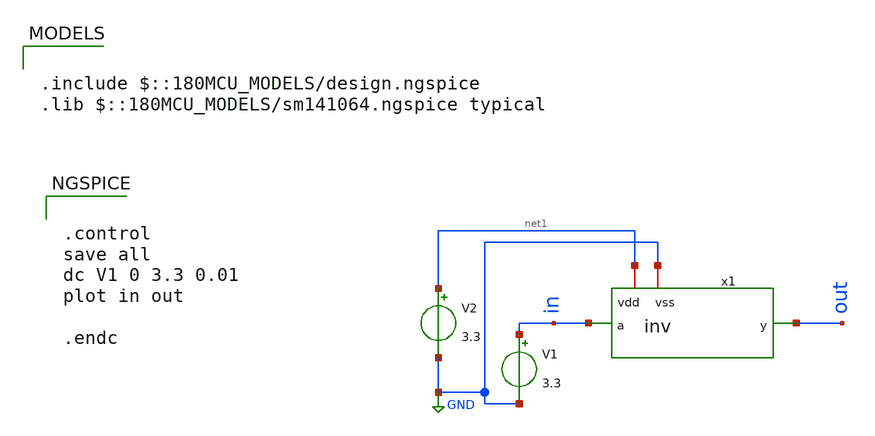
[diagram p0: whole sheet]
** sch_path: member_project/ice458/dynamic_comparator/xschem/inv_tb.sch
**.subckt inv_tb
x1 net1 in out GND inv
V1 in GND 3.3
V2 net1 GND 3.3
**** begin user architecture code

.include $::180MCU_MODELS/design.ngspice
.lib $::180MCU_MODELS/sm141064.ngspice typical



.control
save all
dc V1 0 3.3 0.01
plot in out

.endc


**** end user architecture code
**.ends

* expanding   symbol:  inv.sym # of pins=4
** sym_path: member_project/ice458/dynamic_comparator/xschem/inv.sym
** sch_path: member_project/ice458/dynamic_comparator/xschem/inv.sch
.subckt inv vdd a y vss
*.iopin vdd
*.iopin vss
*.ipin a
*.opin y
XM1 y a vss vss nfet_03v3 L=0.28u W=0.42u nf=1 ad='int((nf+1)/2) * W/nf * 0.18u' as='int((nf+2)/2) * W/nf * 0.18u'
+ pd='2*int((nf+1)/2) * (W/nf + 0.18u)' ps='2*int((nf+2)/2) * (W/nf + 0.18u)' nrd='0.18u / W' nrs='0.18u / W'
+ sa=0 sb=0 sd=0 m=1
XM2 y a vdd vdd pfet_03v3 L=0.28u W=1u nf=1 ad='int((nf+1)/2) * W/nf * 0.18u' as='int((nf+2)/2) * W/nf * 0.18u'
+ pd='2*int((nf+1)/2) * (W/nf + 0.18u)' ps='2*int((nf+2)/2) * (W/nf + 0.18u)' nrd='0.18u / W' nrs='0.18u / W'
+ sa=0 sb=0 sd=0 m=1
.ends

.GLOBAL GND
.end
